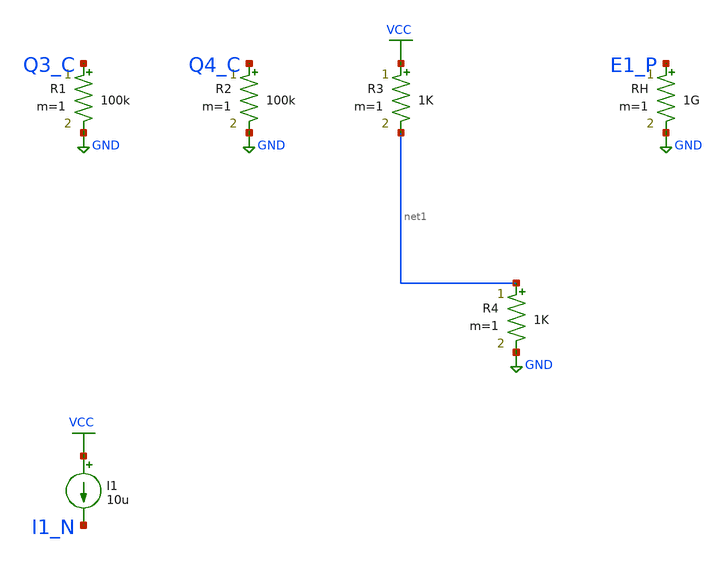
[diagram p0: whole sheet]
** sch_path: data/sch/aicas_diffamp.sch
**.subckt aicas_diffamp
R1 Q3_C GND 100k m=1
R2 Q4_C GND 100k m=1
R3 VCC net1 1K m=1
R4 net1 GND 1K m=1
I1 VCC I1_N 10u
RH E1_P GND 1G m=1
**.ends
.GLOBAL VCC
.GLOBAL GND
.end
